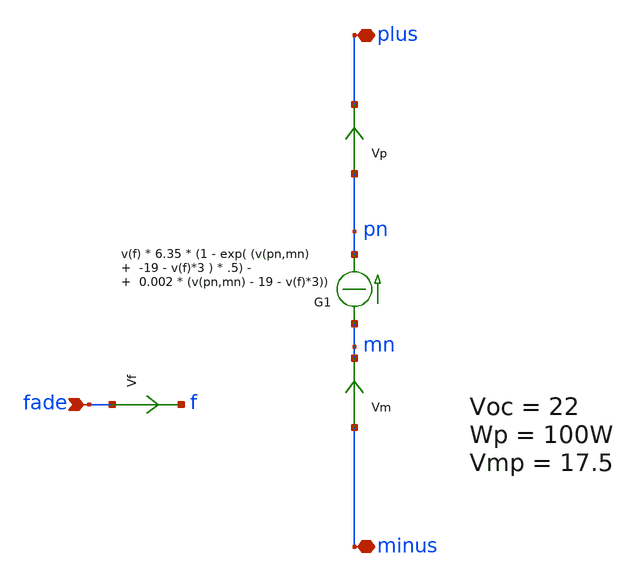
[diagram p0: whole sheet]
** sch_path: xschem_library/ngspice/pv_ngspice.sch
**.subckt pv_ngspice plus minus fade
*.iopin plus
*.iopin minus
*.ipin fade
Vm minus mn 0
.save i(vm)
G1 mn pn CUR=' v(f) * 6.35 * (1 - exp( (v(pn,mn) -19 - v(f)*3 ) * .5) - 0.002 * (v(pn,mn) - 19 - v(f)*3)) '
Vf fade f 0
.save i(vf)
Vp pn plus 0
.save i(vp)
**.ends
.end
